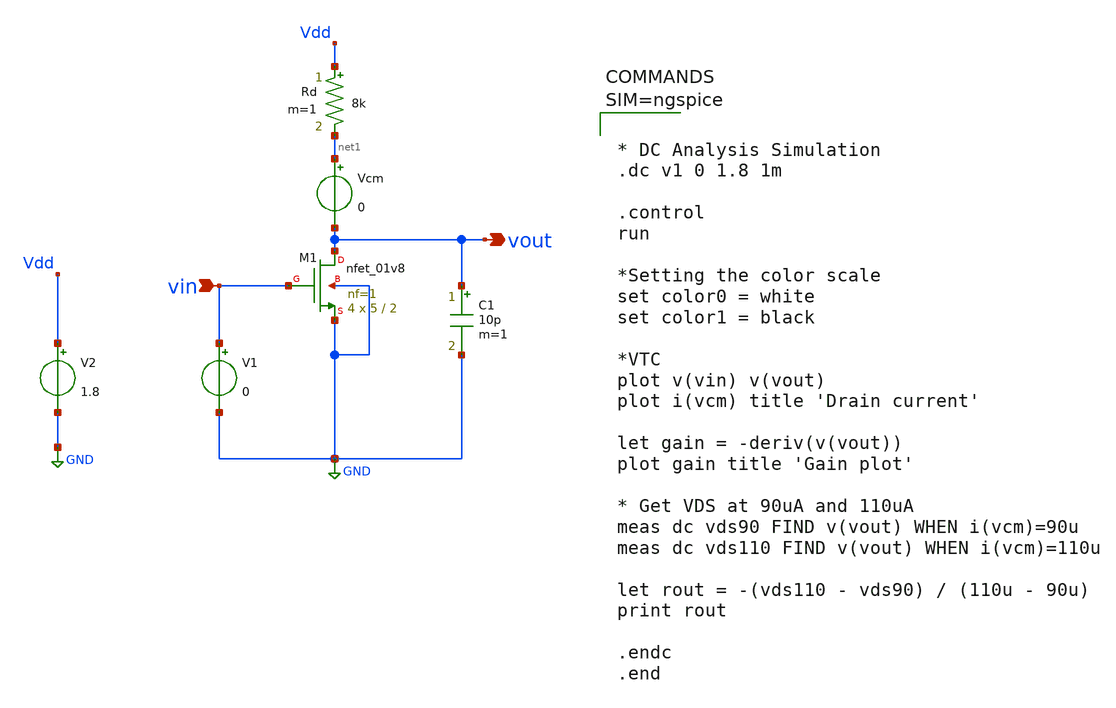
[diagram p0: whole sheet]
** sch_path: Common_Source_Restitive_Load_ckts/NMOS_CS_Amp_Res_load_dc_analysis.sch
**.subckt NMOS_CS_Amp_Res_load_dc_analysis vout vin
*.opin vout
*.ipin vin
XM1 vout vin GND GND sky130_fd_pr__nfet_01v8 L=2 W=5 nf=1 ad='int((1 + 1)/2) * 5 / 1 * 0.29' as='int((1 + 2)/2) * 5 / 1 * 0.29'
+ pd='2*int((1 + 1)/2) * (5 / 1 + 0.29)' ps='2*int((1 + 2)/2) * (5 / 1 + 0.29)' nrd='0.29 / 5 ' nrs='0.29 / 5 '
+ sa=0 sb=0 sd=0 mult=4 m=4
Rd Vdd net1 8k m=1
V1 vin GND 0
V2 Vdd GND 1.8
Vcm net1 vout 0
C1 vout GND 10p m=1
**** begin user architecture code

** opencircuitdesign pdks install
.lib $::SKYWATER_MODELS/sky130.lib.spice tt




* DC Analysis Simulation
.dc v1 0 1.8 1m

.control
run

*Setting the color scale
set color0 = white
set color1 = black

*VTC
plot v(vin) v(vout)
plot i(vcm) title 'Drain current'

let gain = -deriv(v(vout))
plot gain title 'Gain plot'

* Get VDS at 90uA and 110uA
meas dc vds90 FIND v(vout) WHEN i(vcm)=90u
meas dc vds110 FIND v(vout) WHEN i(vcm)=110u

let rout = -(vds110 - vds90) / (110u - 90u)
print rout

.endc
.end




**** end user architecture code
**.ends
.GLOBAL GND
.end
